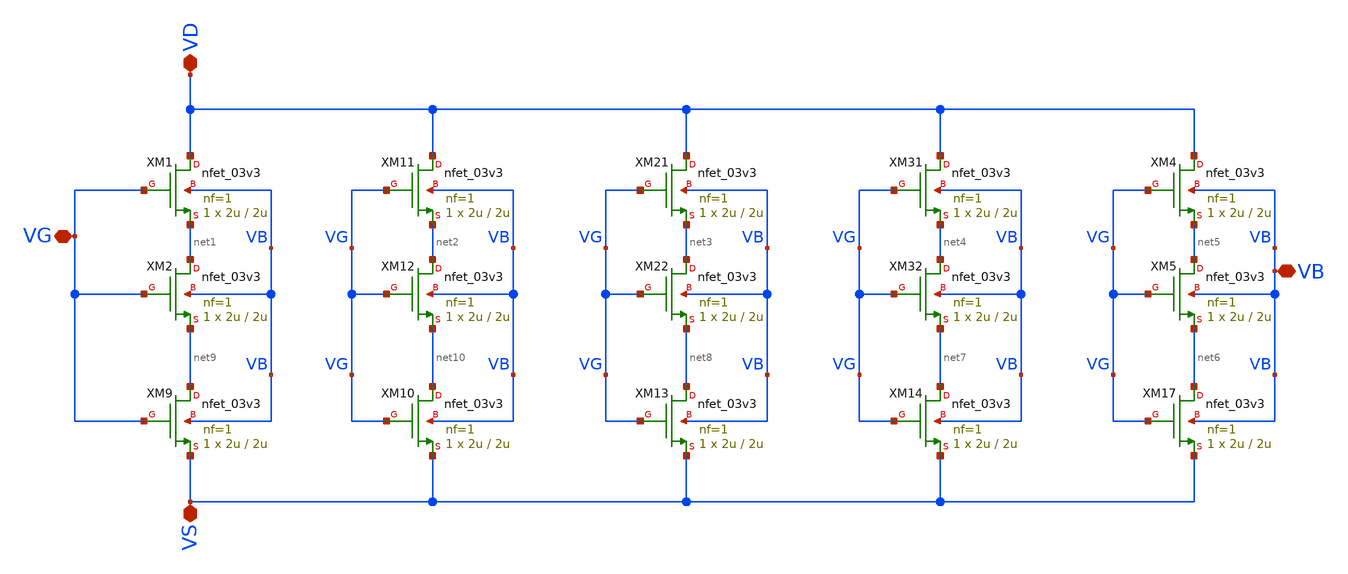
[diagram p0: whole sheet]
** sch_path: Voltage_Reference/symbols/NMOS_association_13u_2u.sch
**.subckt NMOS_association_13u_2u VD VG VS VB
*.iopin VD
*.iopin VG
*.iopin VS
*.iopin VB
XM1 VD VG net1 VB nfet_03v3 L=2u W=2u nf=1 ad='int((nf+1)/2) * W/nf * 0.18u' as='int((nf+2)/2) * W/nf * 0.18u'
+ pd='2*int((nf+1)/2) * (W/nf + 0.18u)' ps='2*int((nf+2)/2) * (W/nf + 0.18u)' nrd='0.18u / W' nrs='0.18u / W'
+ sa=0 sb=0 sd=0 m=1
XM2 net1 VG net9 VB nfet_03v3 L=2u W=2u nf=1 ad='int((nf+1)/2) * W/nf * 0.18u' as='int((nf+2)/2) * W/nf * 0.18u'
+ pd='2*int((nf+1)/2) * (W/nf + 0.18u)' ps='2*int((nf+2)/2) * (W/nf + 0.18u)' nrd='0.18u / W' nrs='0.18u / W'
+ sa=0 sb=0 sd=0 m=1
XM11 VD VG net2 VB nfet_03v3 L=2u W=2u nf=1 ad='int((nf+1)/2) * W/nf * 0.18u' as='int((nf+2)/2) * W/nf * 0.18u'
+ pd='2*int((nf+1)/2) * (W/nf + 0.18u)' ps='2*int((nf+2)/2) * (W/nf + 0.18u)' nrd='0.18u / W' nrs='0.18u / W'
+ sa=0 sb=0 sd=0 m=1
XM12 net2 VG net10 VB nfet_03v3 L=2u W=2u nf=1 ad='int((nf+1)/2) * W/nf * 0.18u' as='int((nf+2)/2) * W/nf * 0.18u'
+ pd='2*int((nf+1)/2) * (W/nf + 0.18u)' ps='2*int((nf+2)/2) * (W/nf + 0.18u)' nrd='0.18u / W' nrs='0.18u / W'
+ sa=0 sb=0 sd=0 m=1
XM21 VD VG net3 VB nfet_03v3 L=2u W=2u nf=1 ad='int((nf+1)/2) * W/nf * 0.18u' as='int((nf+2)/2) * W/nf * 0.18u'
+ pd='2*int((nf+1)/2) * (W/nf + 0.18u)' ps='2*int((nf+2)/2) * (W/nf + 0.18u)' nrd='0.18u / W' nrs='0.18u / W'
+ sa=0 sb=0 sd=0 m=1
XM22 net3 VG net8 VB nfet_03v3 L=2u W=2u nf=1 ad='int((nf+1)/2) * W/nf * 0.18u' as='int((nf+2)/2) * W/nf * 0.18u'
+ pd='2*int((nf+1)/2) * (W/nf + 0.18u)' ps='2*int((nf+2)/2) * (W/nf + 0.18u)' nrd='0.18u / W' nrs='0.18u / W'
+ sa=0 sb=0 sd=0 m=1
XM31 VD VG net4 VB nfet_03v3 L=2u W=2u nf=1 ad='int((nf+1)/2) * W/nf * 0.18u' as='int((nf+2)/2) * W/nf * 0.18u'
+ pd='2*int((nf+1)/2) * (W/nf + 0.18u)' ps='2*int((nf+2)/2) * (W/nf + 0.18u)' nrd='0.18u / W' nrs='0.18u / W'
+ sa=0 sb=0 sd=0 m=1
XM32 net4 VG net7 VB nfet_03v3 L=2u W=2u nf=1 ad='int((nf+1)/2) * W/nf * 0.18u' as='int((nf+2)/2) * W/nf * 0.18u'
+ pd='2*int((nf+1)/2) * (W/nf + 0.18u)' ps='2*int((nf+2)/2) * (W/nf + 0.18u)' nrd='0.18u / W' nrs='0.18u / W'
+ sa=0 sb=0 sd=0 m=1
XM4 VD VG net5 VB nfet_03v3 L=2u W=2u nf=1 ad='int((nf+1)/2) * W/nf * 0.18u' as='int((nf+2)/2) * W/nf * 0.18u'
+ pd='2*int((nf+1)/2) * (W/nf + 0.18u)' ps='2*int((nf+2)/2) * (W/nf + 0.18u)' nrd='0.18u / W' nrs='0.18u / W'
+ sa=0 sb=0 sd=0 m=1
XM5 net5 VG net6 VB nfet_03v3 L=2u W=2u nf=1 ad='int((nf+1)/2) * W/nf * 0.18u' as='int((nf+2)/2) * W/nf * 0.18u'
+ pd='2*int((nf+1)/2) * (W/nf + 0.18u)' ps='2*int((nf+2)/2) * (W/nf + 0.18u)' nrd='0.18u / W' nrs='0.18u / W'
+ sa=0 sb=0 sd=0 m=1
XM9 net9 VG VS VB nfet_03v3 L=2u W=2u nf=1 ad='int((nf+1)/2) * W/nf * 0.18u' as='int((nf+2)/2) * W/nf * 0.18u'
+ pd='2*int((nf+1)/2) * (W/nf + 0.18u)' ps='2*int((nf+2)/2) * (W/nf + 0.18u)' nrd='0.18u / W' nrs='0.18u / W'
+ sa=0 sb=0 sd=0 m=1
XM10 net10 VG VS VB nfet_03v3 L=2u W=2u nf=1 ad='int((nf+1)/2) * W/nf * 0.18u' as='int((nf+2)/2) * W/nf * 0.18u'
+ pd='2*int((nf+1)/2) * (W/nf + 0.18u)' ps='2*int((nf+2)/2) * (W/nf + 0.18u)' nrd='0.18u / W' nrs='0.18u / W'
+ sa=0 sb=0 sd=0 m=1
XM13 net8 VG VS VB nfet_03v3 L=2u W=2u nf=1 ad='int((nf+1)/2) * W/nf * 0.18u' as='int((nf+2)/2) * W/nf * 0.18u'
+ pd='2*int((nf+1)/2) * (W/nf + 0.18u)' ps='2*int((nf+2)/2) * (W/nf + 0.18u)' nrd='0.18u / W' nrs='0.18u / W'
+ sa=0 sb=0 sd=0 m=1
XM14 net7 VG VS VB nfet_03v3 L=2u W=2u nf=1 ad='int((nf+1)/2) * W/nf * 0.18u' as='int((nf+2)/2) * W/nf * 0.18u'
+ pd='2*int((nf+1)/2) * (W/nf + 0.18u)' ps='2*int((nf+2)/2) * (W/nf + 0.18u)' nrd='0.18u / W' nrs='0.18u / W'
+ sa=0 sb=0 sd=0 m=1
XM17 net6 VG VS VB nfet_03v3 L=2u W=2u nf=1 ad='int((nf+1)/2) * W/nf * 0.18u' as='int((nf+2)/2) * W/nf * 0.18u'
+ pd='2*int((nf+1)/2) * (W/nf + 0.18u)' ps='2*int((nf+2)/2) * (W/nf + 0.18u)' nrd='0.18u / W' nrs='0.18u / W'
+ sa=0 sb=0 sd=0 m=1
**.ends
.end
